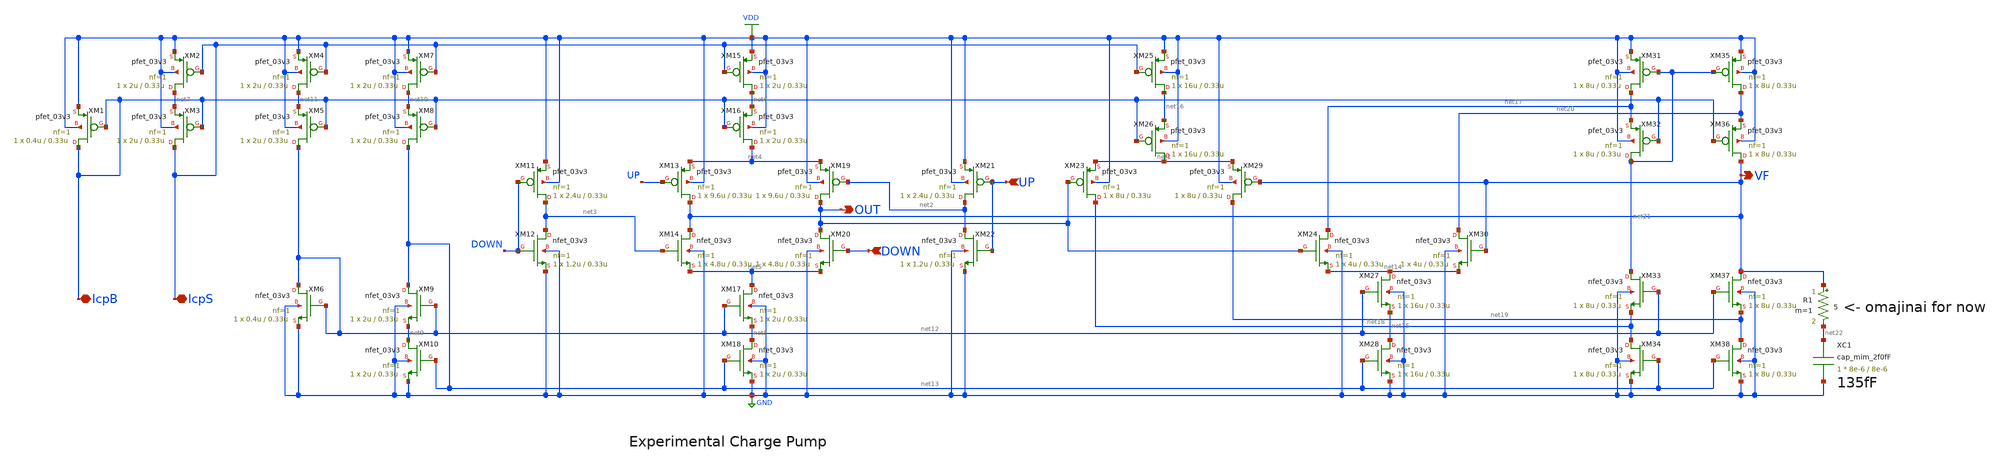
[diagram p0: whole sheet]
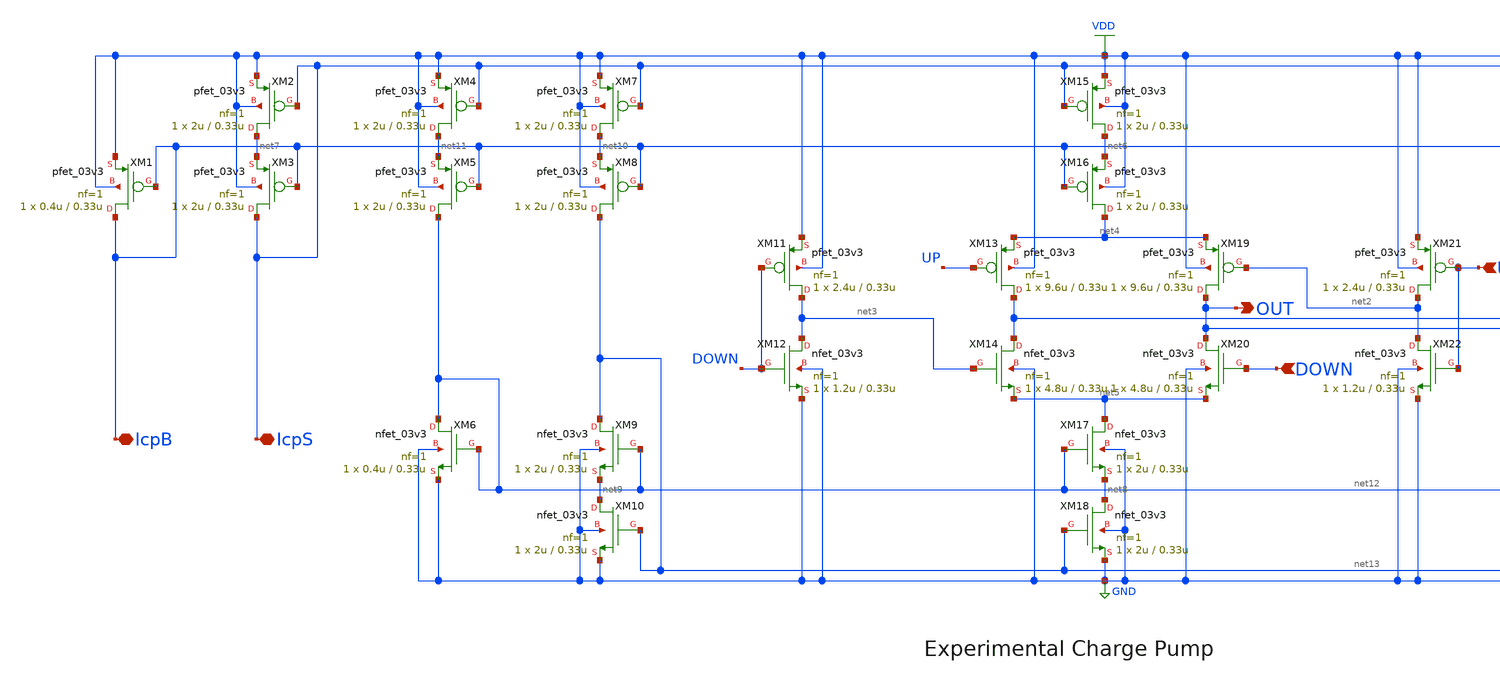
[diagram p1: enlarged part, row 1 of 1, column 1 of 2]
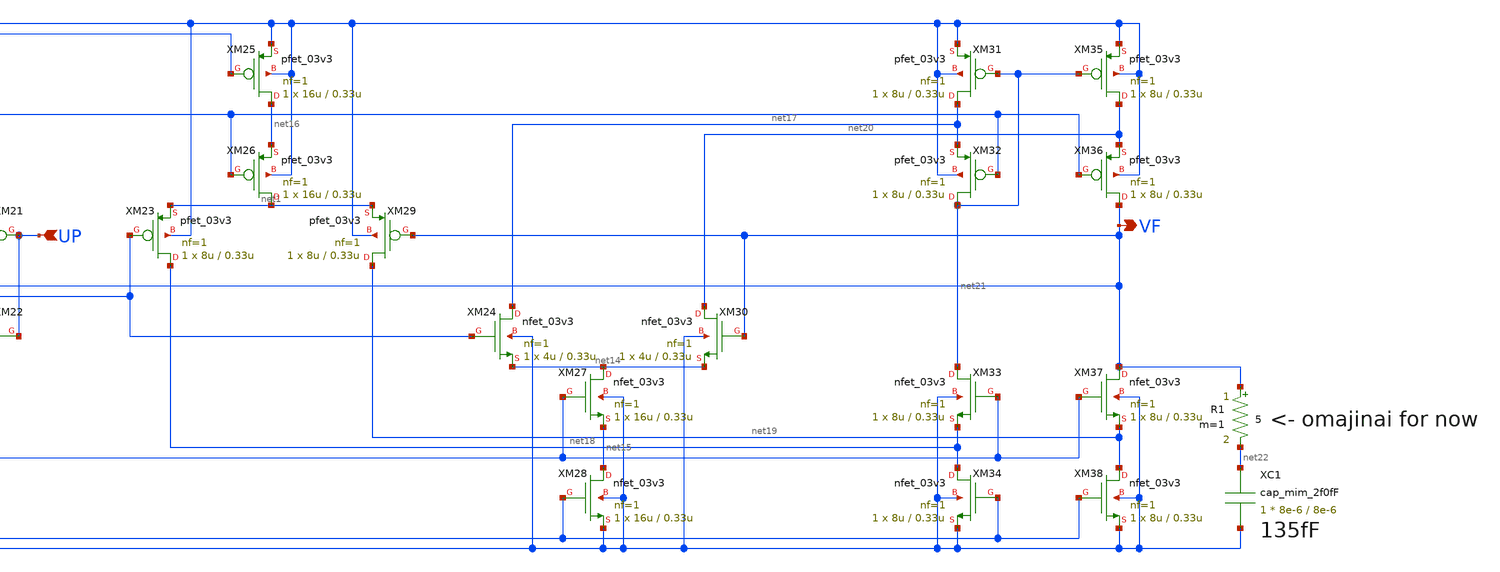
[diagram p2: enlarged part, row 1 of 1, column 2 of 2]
** sch_path: cp.sch
**.subckt cp IcpS IcpB DOWN UP OUT VF
*.iopin IcpS
*.iopin IcpB
*.ipin DOWN
*.ipin UP
*.opin OUT
*.opin VF
XM23 net18 OUT net1 VDD pfet_03v3 L=0.33u W=8u nf=1 ad='int((nf+1)/2) * W/nf * 0.18u' as='int((nf+2)/2) * W/nf * 0.18u'
+ pd='2*int((nf+1)/2) * (W/nf + 0.18u)' ps='2*int((nf+2)/2) * (W/nf + 0.18u)' nrd='0.18u / W' nrs='0.18u / W'
+ sa=0 sb=0 sd=0 m=1
XM29 net19 VF net1 VDD pfet_03v3 L=0.33u W=8u nf=1 ad='int((nf+1)/2) * W/nf * 0.18u' as='int((nf+2)/2) * W/nf * 0.18u'
+ pd='2*int((nf+1)/2) * (W/nf + 0.18u)' ps='2*int((nf+2)/2) * (W/nf + 0.18u)' nrd='0.18u / W' nrs='0.18u / W'
+ sa=0 sb=0 sd=0 m=1
XM19 OUT net2 net4 VDD pfet_03v3 L=0.33u W=9.6u nf=1 ad='int((nf+1)/2) * W/nf * 0.18u' as='int((nf+2)/2) * W/nf * 0.18u'
+ pd='2*int((nf+1)/2) * (W/nf + 0.18u)' ps='2*int((nf+2)/2) * (W/nf + 0.18u)' nrd='0.18u / W' nrs='0.18u / W'
+ sa=0 sb=0 sd=0 m=1
XM20 OUT DOWN net5 GND nfet_03v3 L=0.33u W=4.8u nf=1 ad='int((nf+1)/2) * W/nf * 0.18u' as='int((nf+2)/2) * W/nf * 0.18u'
+ pd='2*int((nf+1)/2) * (W/nf + 0.18u)' ps='2*int((nf+2)/2) * (W/nf + 0.18u)' nrd='0.18u / W' nrs='0.18u / W'
+ sa=0 sb=0 sd=0 m=1
XM21 net2 UP VDD VDD pfet_03v3 L=0.33u W=2.4u nf=1 ad='int((nf+1)/2) * W/nf * 0.18u' as='int((nf+2)/2) * W/nf * 0.18u'
+ pd='2*int((nf+1)/2) * (W/nf + 0.18u)' ps='2*int((nf+2)/2) * (W/nf + 0.18u)' nrd='0.18u / W' nrs='0.18u / W'
+ sa=0 sb=0 sd=0 m=1
XM22 net2 UP GND GND nfet_03v3 L=0.33u W=1.2u nf=1 ad='int((nf+1)/2) * W/nf * 0.18u' as='int((nf+2)/2) * W/nf * 0.18u'
+ pd='2*int((nf+1)/2) * (W/nf + 0.18u)' ps='2*int((nf+2)/2) * (W/nf + 0.18u)' nrd='0.18u / W' nrs='0.18u / W'
+ sa=0 sb=0 sd=0 m=1
XM13 VF UP net4 VDD pfet_03v3 L=0.33u W=9.6u nf=1 ad='int((nf+1)/2) * W/nf * 0.18u' as='int((nf+2)/2) * W/nf * 0.18u'
+ pd='2*int((nf+1)/2) * (W/nf + 0.18u)' ps='2*int((nf+2)/2) * (W/nf + 0.18u)' nrd='0.18u / W' nrs='0.18u / W'
+ sa=0 sb=0 sd=0 m=1
XM14 VF net3 net5 GND nfet_03v3 L=0.33u W=4.8u nf=1 ad='int((nf+1)/2) * W/nf * 0.18u' as='int((nf+2)/2) * W/nf * 0.18u'
+ pd='2*int((nf+1)/2) * (W/nf + 0.18u)' ps='2*int((nf+2)/2) * (W/nf + 0.18u)' nrd='0.18u / W' nrs='0.18u / W'
+ sa=0 sb=0 sd=0 m=1
XM11 net3 DOWN VDD VDD pfet_03v3 L=0.33u W=2.4u nf=1 ad='int((nf+1)/2) * W/nf * 0.18u' as='int((nf+2)/2) * W/nf * 0.18u'
+ pd='2*int((nf+1)/2) * (W/nf + 0.18u)' ps='2*int((nf+2)/2) * (W/nf + 0.18u)' nrd='0.18u / W' nrs='0.18u / W'
+ sa=0 sb=0 sd=0 m=1
XM12 net3 DOWN GND GND nfet_03v3 L=0.33u W=1.2u nf=1 ad='int((nf+1)/2) * W/nf * 0.18u' as='int((nf+2)/2) * W/nf * 0.18u'
+ pd='2*int((nf+1)/2) * (W/nf + 0.18u)' ps='2*int((nf+2)/2) * (W/nf + 0.18u)' nrd='0.18u / W' nrs='0.18u / W'
+ sa=0 sb=0 sd=0 m=1
XM17 net5 net12 net8 GND nfet_03v3 L=0.33u W=2u nf=1 ad='int((nf+1)/2) * W/nf * 0.18u' as='int((nf+2)/2) * W/nf * 0.18u'
+ pd='2*int((nf+1)/2) * (W/nf + 0.18u)' ps='2*int((nf+2)/2) * (W/nf + 0.18u)' nrd='0.18u / W' nrs='0.18u / W'
+ sa=0 sb=0 sd=0 m=1
XM18 net8 net13 GND GND nfet_03v3 L=0.33u W=2u nf=1 ad='int((nf+1)/2) * W/nf * 0.18u' as='int((nf+2)/2) * W/nf * 0.18u'
+ pd='2*int((nf+1)/2) * (W/nf + 0.18u)' ps='2*int((nf+2)/2) * (W/nf + 0.18u)' nrd='0.18u / W' nrs='0.18u / W'
+ sa=0 sb=0 sd=0 m=1
XM15 net6 IcpS VDD VDD pfet_03v3 L=0.33u W=2u nf=1 ad='int((nf+1)/2) * W/nf * 0.18u' as='int((nf+2)/2) * W/nf * 0.18u'
+ pd='2*int((nf+1)/2) * (W/nf + 0.18u)' ps='2*int((nf+2)/2) * (W/nf + 0.18u)' nrd='0.18u / W' nrs='0.18u / W'
+ sa=0 sb=0 sd=0 m=1
XM16 net4 IcpB net6 VDD pfet_03v3 L=0.33u W=2u nf=1 ad='int((nf+1)/2) * W/nf * 0.18u' as='int((nf+2)/2) * W/nf * 0.18u'
+ pd='2*int((nf+1)/2) * (W/nf + 0.18u)' ps='2*int((nf+2)/2) * (W/nf + 0.18u)' nrd='0.18u / W' nrs='0.18u / W'
+ sa=0 sb=0 sd=0 m=1
XM25 net16 IcpS VDD VDD pfet_03v3 L=0.33u W=16u nf=1 ad='int((nf+1)/2) * W/nf * 0.18u' as='int((nf+2)/2) * W/nf * 0.18u'
+ pd='2*int((nf+1)/2) * (W/nf + 0.18u)' ps='2*int((nf+2)/2) * (W/nf + 0.18u)' nrd='0.18u / W' nrs='0.18u / W'
+ sa=0 sb=0 sd=0 m=1
XM26 net1 IcpB net16 VDD pfet_03v3 L=0.33u W=16u nf=1 ad='int((nf+1)/2) * W/nf * 0.18u' as='int((nf+2)/2) * W/nf * 0.18u'
+ pd='2*int((nf+1)/2) * (W/nf + 0.18u)' ps='2*int((nf+2)/2) * (W/nf + 0.18u)' nrd='0.18u / W' nrs='0.18u / W'
+ sa=0 sb=0 sd=0 m=1
XM2 net7 IcpS VDD VDD pfet_03v3 L=0.33u W=2u nf=1 ad='int((nf+1)/2) * W/nf * 0.18u' as='int((nf+2)/2) * W/nf * 0.18u'
+ pd='2*int((nf+1)/2) * (W/nf + 0.18u)' ps='2*int((nf+2)/2) * (W/nf + 0.18u)' nrd='0.18u / W' nrs='0.18u / W'
+ sa=0 sb=0 sd=0 m=1
XM3 IcpS IcpB net7 VDD pfet_03v3 L=0.33u W=2u nf=1 ad='int((nf+1)/2) * W/nf * 0.18u' as='int((nf+2)/2) * W/nf * 0.18u'
+ pd='2*int((nf+1)/2) * (W/nf + 0.18u)' ps='2*int((nf+2)/2) * (W/nf + 0.18u)' nrd='0.18u / W' nrs='0.18u / W'
+ sa=0 sb=0 sd=0 m=1
XM1 IcpB IcpB VDD VDD pfet_03v3 L=0.33u W=0.4u nf=1 ad='int((nf+1)/2) * W/nf * 0.18u' as='int((nf+2)/2) * W/nf * 0.18u'
+ pd='2*int((nf+1)/2) * (W/nf + 0.18u)' ps='2*int((nf+2)/2) * (W/nf + 0.18u)' nrd='0.18u / W' nrs='0.18u / W'
+ sa=0 sb=0 sd=0 m=1
XM9 net13 net12 net9 GND nfet_03v3 L=0.33u W=2u nf=1 ad='int((nf+1)/2) * W/nf * 0.18u' as='int((nf+2)/2) * W/nf * 0.18u'
+ pd='2*int((nf+1)/2) * (W/nf + 0.18u)' ps='2*int((nf+2)/2) * (W/nf + 0.18u)' nrd='0.18u / W' nrs='0.18u / W'
+ sa=0 sb=0 sd=0 m=1
XM10 net9 net13 GND GND nfet_03v3 L=0.33u W=2u nf=1 ad='int((nf+1)/2) * W/nf * 0.18u' as='int((nf+2)/2) * W/nf * 0.18u'
+ pd='2*int((nf+1)/2) * (W/nf + 0.18u)' ps='2*int((nf+2)/2) * (W/nf + 0.18u)' nrd='0.18u / W' nrs='0.18u / W'
+ sa=0 sb=0 sd=0 m=1
XM7 net10 IcpS VDD VDD pfet_03v3 L=0.33u W=2u nf=1 ad='int((nf+1)/2) * W/nf * 0.18u' as='int((nf+2)/2) * W/nf * 0.18u'
+ pd='2*int((nf+1)/2) * (W/nf + 0.18u)' ps='2*int((nf+2)/2) * (W/nf + 0.18u)' nrd='0.18u / W' nrs='0.18u / W'
+ sa=0 sb=0 sd=0 m=1
XM8 net13 IcpB net10 VDD pfet_03v3 L=0.33u W=2u nf=1 ad='int((nf+1)/2) * W/nf * 0.18u' as='int((nf+2)/2) * W/nf * 0.18u'
+ pd='2*int((nf+1)/2) * (W/nf + 0.18u)' ps='2*int((nf+2)/2) * (W/nf + 0.18u)' nrd='0.18u / W' nrs='0.18u / W'
+ sa=0 sb=0 sd=0 m=1
XM4 net11 IcpS VDD VDD pfet_03v3 L=0.33u W=2u nf=1 ad='int((nf+1)/2) * W/nf * 0.18u' as='int((nf+2)/2) * W/nf * 0.18u'
+ pd='2*int((nf+1)/2) * (W/nf + 0.18u)' ps='2*int((nf+2)/2) * (W/nf + 0.18u)' nrd='0.18u / W' nrs='0.18u / W'
+ sa=0 sb=0 sd=0 m=1
XM5 net12 IcpB net11 VDD pfet_03v3 L=0.33u W=2u nf=1 ad='int((nf+1)/2) * W/nf * 0.18u' as='int((nf+2)/2) * W/nf * 0.18u'
+ pd='2*int((nf+1)/2) * (W/nf + 0.18u)' ps='2*int((nf+2)/2) * (W/nf + 0.18u)' nrd='0.18u / W' nrs='0.18u / W'
+ sa=0 sb=0 sd=0 m=1
XM6 net12 net12 GND GND nfet_03v3 L=0.33u W=0.4u nf=1 ad='int((nf+1)/2) * W/nf * 0.18u' as='int((nf+2)/2) * W/nf * 0.18u'
+ pd='2*int((nf+1)/2) * (W/nf + 0.18u)' ps='2*int((nf+2)/2) * (W/nf + 0.18u)' nrd='0.18u / W' nrs='0.18u / W'
+ sa=0 sb=0 sd=0 m=1
XM33 net21 net12 net18 GND nfet_03v3 L=0.33u W=8u nf=1 ad='int((nf+1)/2) * W/nf * 0.18u' as='int((nf+2)/2) * W/nf * 0.18u'
+ pd='2*int((nf+1)/2) * (W/nf + 0.18u)' ps='2*int((nf+2)/2) * (W/nf + 0.18u)' nrd='0.18u / W' nrs='0.18u / W'
+ sa=0 sb=0 sd=0 m=1
XM31 net17 net21 VDD VDD pfet_03v3 L=0.33u W=8u nf=1 ad='int((nf+1)/2) * W/nf * 0.18u' as='int((nf+2)/2) * W/nf * 0.18u'
+ pd='2*int((nf+1)/2) * (W/nf + 0.18u)' ps='2*int((nf+2)/2) * (W/nf + 0.18u)' nrd='0.18u / W' nrs='0.18u / W'
+ sa=0 sb=0 sd=0 m=1
XM32 net21 IcpB net17 VDD pfet_03v3 L=0.33u W=8u nf=1 ad='int((nf+1)/2) * W/nf * 0.18u' as='int((nf+2)/2) * W/nf * 0.18u'
+ pd='2*int((nf+1)/2) * (W/nf + 0.18u)' ps='2*int((nf+2)/2) * (W/nf + 0.18u)' nrd='0.18u / W' nrs='0.18u / W'
+ sa=0 sb=0 sd=0 m=1
XM34 net18 net13 GND GND nfet_03v3 L=0.33u W=8u nf=1 ad='int((nf+1)/2) * W/nf * 0.18u' as='int((nf+2)/2) * W/nf * 0.18u'
+ pd='2*int((nf+1)/2) * (W/nf + 0.18u)' ps='2*int((nf+2)/2) * (W/nf + 0.18u)' nrd='0.18u / W' nrs='0.18u / W'
+ sa=0 sb=0 sd=0 m=1
XM35 net20 net21 VDD VDD pfet_03v3 L=0.33u W=8u nf=1 ad='int((nf+1)/2) * W/nf * 0.18u' as='int((nf+2)/2) * W/nf * 0.18u'
+ pd='2*int((nf+1)/2) * (W/nf + 0.18u)' ps='2*int((nf+2)/2) * (W/nf + 0.18u)' nrd='0.18u / W' nrs='0.18u / W'
+ sa=0 sb=0 sd=0 m=1
XM36 VF IcpB net20 VDD pfet_03v3 L=0.33u W=8u nf=1 ad='int((nf+1)/2) * W/nf * 0.18u' as='int((nf+2)/2) * W/nf * 0.18u'
+ pd='2*int((nf+1)/2) * (W/nf + 0.18u)' ps='2*int((nf+2)/2) * (W/nf + 0.18u)' nrd='0.18u / W' nrs='0.18u / W'
+ sa=0 sb=0 sd=0 m=1
XM37 VF net12 net19 GND nfet_03v3 L=0.33u W=8u nf=1 ad='int((nf+1)/2) * W/nf * 0.18u' as='int((nf+2)/2) * W/nf * 0.18u'
+ pd='2*int((nf+1)/2) * (W/nf + 0.18u)' ps='2*int((nf+2)/2) * (W/nf + 0.18u)' nrd='0.18u / W' nrs='0.18u / W'
+ sa=0 sb=0 sd=0 m=1
XM38 net19 net13 GND GND nfet_03v3 L=0.33u W=8u nf=1 ad='int((nf+1)/2) * W/nf * 0.18u' as='int((nf+2)/2) * W/nf * 0.18u'
+ pd='2*int((nf+1)/2) * (W/nf + 0.18u)' ps='2*int((nf+2)/2) * (W/nf + 0.18u)' nrd='0.18u / W' nrs='0.18u / W'
+ sa=0 sb=0 sd=0 m=1
XM27 net14 net12 net15 GND nfet_03v3 L=0.33u W=16u nf=1 ad='int((nf+1)/2) * W/nf * 0.18u' as='int((nf+2)/2) * W/nf * 0.18u'
+ pd='2*int((nf+1)/2) * (W/nf + 0.18u)' ps='2*int((nf+2)/2) * (W/nf + 0.18u)' nrd='0.18u / W' nrs='0.18u / W'
+ sa=0 sb=0 sd=0 m=1
XM28 net15 net13 GND GND nfet_03v3 L=0.33u W=16u nf=1 ad='int((nf+1)/2) * W/nf * 0.18u' as='int((nf+2)/2) * W/nf * 0.18u'
+ pd='2*int((nf+1)/2) * (W/nf + 0.18u)' ps='2*int((nf+2)/2) * (W/nf + 0.18u)' nrd='0.18u / W' nrs='0.18u / W'
+ sa=0 sb=0 sd=0 m=1
XM24 net17 OUT net14 GND nfet_03v3 L=0.33u W=4u nf=1 ad='int((nf+1)/2) * W/nf * 0.18u' as='int((nf+2)/2) * W/nf * 0.18u'
+ pd='2*int((nf+1)/2) * (W/nf + 0.18u)' ps='2*int((nf+2)/2) * (W/nf + 0.18u)' nrd='0.18u / W' nrs='0.18u / W'
+ sa=0 sb=0 sd=0 m=1
XM30 net20 VF net14 GND nfet_03v3 L=0.33u W=4u nf=1 ad='int((nf+1)/2) * W/nf * 0.18u' as='int((nf+2)/2) * W/nf * 0.18u'
+ pd='2*int((nf+1)/2) * (W/nf + 0.18u)' ps='2*int((nf+2)/2) * (W/nf + 0.18u)' nrd='0.18u / W' nrs='0.18u / W'
+ sa=0 sb=0 sd=0 m=1
XC1 net22 GND cap_mim_2f0fF c_width=8e-6 c_length=8e-6 m=1
R1 VF net22 5 m=1
**.ends
.GLOBAL VDD
.GLOBAL GND
.end
